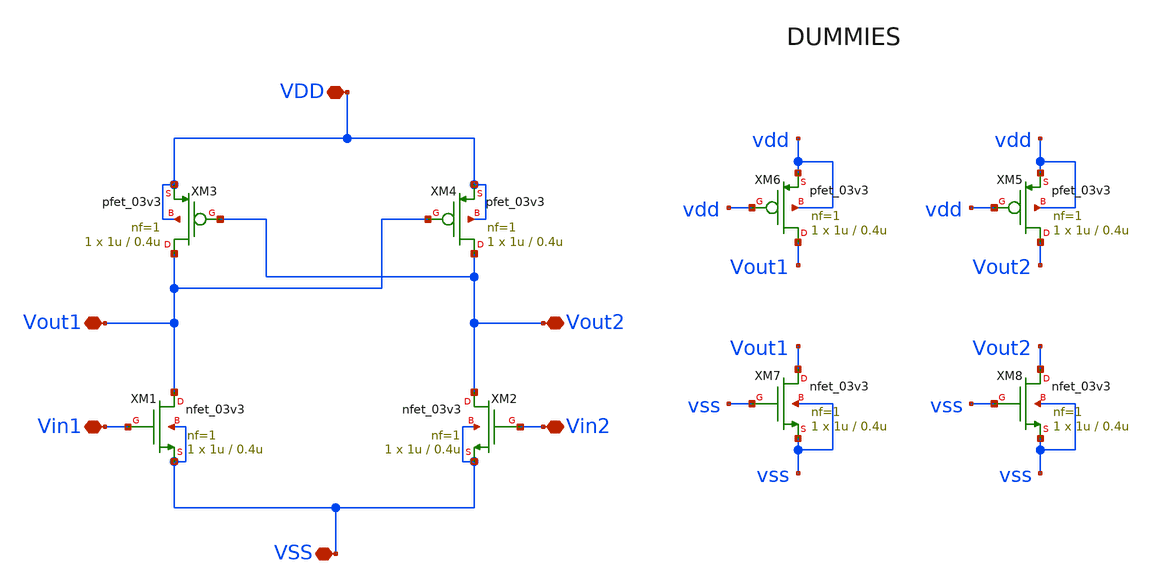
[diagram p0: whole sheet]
** sch_path: Analog/schematics/3_comparator/rslatch.sch
**.subckt rslatch VDD VSS Vin1 Vin2 Vout1 Vout2
*.iopin VDD
*.iopin VSS
*.iopin Vin1
*.iopin Vin2
*.iopin Vout1
*.iopin Vout2
XM1 Vout1 Vin1 VSS VSS nfet_03v3 L=0.4u W=1u nf=1 ad='int((nf+1)/2) * W/nf * 0.18u' as='int((nf+2)/2) * W/nf * 0.18u'
+ pd='2*int((nf+1)/2) * (W/nf + 0.18u)' ps='2*int((nf+2)/2) * (W/nf + 0.18u)' nrd='0.18u / W' nrs='0.18u / W'
+ sa=0 sb=0 sd=0 m=1
XM2 Vout2 Vin2 VSS VSS nfet_03v3 L=0.4u W=1u nf=1 ad='int((nf+1)/2) * W/nf * 0.18u' as='int((nf+2)/2) * W/nf * 0.18u'
+ pd='2*int((nf+1)/2) * (W/nf + 0.18u)' ps='2*int((nf+2)/2) * (W/nf + 0.18u)' nrd='0.18u / W' nrs='0.18u / W'
+ sa=0 sb=0 sd=0 m=1
XM3 Vout1 Vout2 VDD VDD pfet_03v3 L=0.4u W=1u nf=1 ad='int((nf+1)/2) * W/nf * 0.18u' as='int((nf+2)/2) * W/nf * 0.18u'
+ pd='2*int((nf+1)/2) * (W/nf + 0.18u)' ps='2*int((nf+2)/2) * (W/nf + 0.18u)' nrd='0.18u / W' nrs='0.18u / W'
+ sa=0 sb=0 sd=0 m=1
XM4 Vout2 Vout1 VDD VDD pfet_03v3 L=0.4u W=1u nf=1 ad='int((nf+1)/2) * W/nf * 0.18u' as='int((nf+2)/2) * W/nf * 0.18u'
+ pd='2*int((nf+1)/2) * (W/nf + 0.18u)' ps='2*int((nf+2)/2) * (W/nf + 0.18u)' nrd='0.18u / W' nrs='0.18u / W'
+ sa=0 sb=0 sd=0 m=1
XM6 Vout1 vdd vdd vdd pfet_03v3 L=0.4u W=1u nf=1 ad='int((nf+1)/2) * W/nf * 0.18u' as='int((nf+2)/2) * W/nf * 0.18u'
+ pd='2*int((nf+1)/2) * (W/nf + 0.18u)' ps='2*int((nf+2)/2) * (W/nf + 0.18u)' nrd='0.18u / W' nrs='0.18u / W'
+ sa=0 sb=0 sd=0 m=1
XM5 Vout2 vdd vdd vdd pfet_03v3 L=0.4u W=1u nf=1 ad='int((nf+1)/2) * W/nf * 0.18u' as='int((nf+2)/2) * W/nf * 0.18u'
+ pd='2*int((nf+1)/2) * (W/nf + 0.18u)' ps='2*int((nf+2)/2) * (W/nf + 0.18u)' nrd='0.18u / W' nrs='0.18u / W'
+ sa=0 sb=0 sd=0 m=1
XM7 Vout1 vss vss vss nfet_03v3 L=0.4u W=1u nf=1 ad='int((nf+1)/2) * W/nf * 0.18u' as='int((nf+2)/2) * W/nf * 0.18u'
+ pd='2*int((nf+1)/2) * (W/nf + 0.18u)' ps='2*int((nf+2)/2) * (W/nf + 0.18u)' nrd='0.18u / W' nrs='0.18u / W'
+ sa=0 sb=0 sd=0 m=1
XM8 Vout2 vss vss vss nfet_03v3 L=0.4u W=1u nf=1 ad='int((nf+1)/2) * W/nf * 0.18u' as='int((nf+2)/2) * W/nf * 0.18u'
+ pd='2*int((nf+1)/2) * (W/nf + 0.18u)' ps='2*int((nf+2)/2) * (W/nf + 0.18u)' nrd='0.18u / W' nrs='0.18u / W'
+ sa=0 sb=0 sd=0 m=1
**.ends
.end
